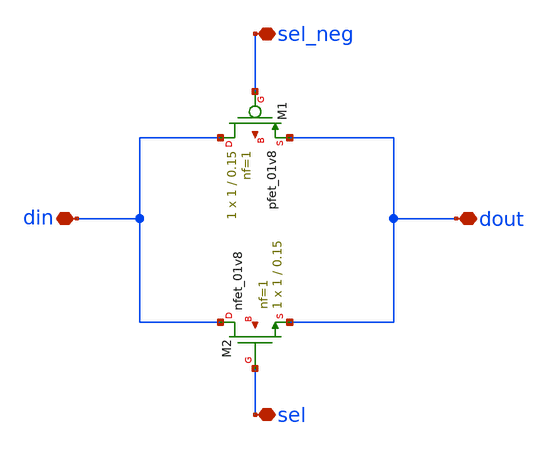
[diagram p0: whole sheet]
** sch_path: tseng_workspace/transmission_gate/schematic/spice/tg_cell.sch
**.subckt tg_cell din dout sel sel_neg
*.iopin din
*.iopin dout
*.iopin sel
*.iopin sel_neg
XM1 din sel_neg dout net1 sky130_fd_pr__pfet_01v8 L=0.15 W=1 nf=1 ad='int((nf+1)/2) * W/nf * 0.29' as='int((nf+2)/2) * W/nf * 0.29'
+ pd='2*int((nf+1)/2) * (W/nf + 0.29)' ps='2*int((nf+2)/2) * (W/nf + 0.29)' nrd='0.29 / W' nrs='0.29 / W'
+ sa=0 sb=0 sd=0 mult=1 m=1
XM2 din sel dout net2 sky130_fd_pr__nfet_01v8 L=0.15 W=1 nf=1 ad='int((nf+1)/2) * W/nf * 0.29' as='int((nf+2)/2) * W/nf * 0.29'
+ pd='2*int((nf+1)/2) * (W/nf + 0.29)' ps='2*int((nf+2)/2) * (W/nf + 0.29)' nrd='0.29 / W' nrs='0.29 / W'
+ sa=0 sb=0 sd=0 mult=1 m=1
**.ends
.end
